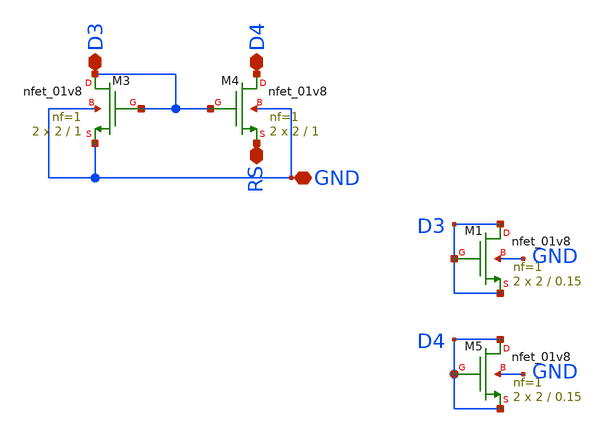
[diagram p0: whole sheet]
** sch_path: opamp/mag/nmoscs/nmoscs.sch
**.subckt nmoscs RS D3 D4 GND
*.iopin RS
*.iopin D3
*.iopin D4
*.iopin GND
XM3 D3 D3 GND GND sky130_fd_pr__nfet_01v8 L=1 W=2 nf=1 ad='int((nf+1)/2) * W/nf * 0.29' as='int((nf+2)/2) * W/nf * 0.29'
+ pd='2*int((nf+1)/2) * (W/nf + 0.29)' ps='2*int((nf+2)/2) * (W/nf + 0.29)' nrd='0.29 / W' nrs='0.29 / W'
+ sa=0 sb=0 sd=0 mult=2 m=2
XM4 D4 D3 RS GND sky130_fd_pr__nfet_01v8 L=1 W=2 nf=1 ad='int((nf+1)/2) * W/nf * 0.29' as='int((nf+2)/2) * W/nf * 0.29'
+ pd='2*int((nf+1)/2) * (W/nf + 0.29)' ps='2*int((nf+2)/2) * (W/nf + 0.29)' nrd='0.29 / W' nrs='0.29 / W'
+ sa=0 sb=0 sd=0 mult=2 m=2
XM1 D3 D3 D3 GND sky130_fd_pr__nfet_01v8 L=0.15 W=2 nf=1 ad='int((nf+1)/2) * W/nf * 0.29' as='int((nf+2)/2) * W/nf * 0.29'
+ pd='2*int((nf+1)/2) * (W/nf + 0.29)' ps='2*int((nf+2)/2) * (W/nf + 0.29)' nrd='0.29 / W' nrs='0.29 / W'
+ sa=0 sb=0 sd=0 mult=2 m=2
XM5 D4 D4 D4 GND sky130_fd_pr__nfet_01v8 L=0.15 W=2 nf=1 ad='int((nf+1)/2) * W/nf * 0.29' as='int((nf+2)/2) * W/nf * 0.29'
+ pd='2*int((nf+1)/2) * (W/nf + 0.29)' ps='2*int((nf+2)/2) * (W/nf + 0.29)' nrd='0.29 / W' nrs='0.29 / W'
+ sa=0 sb=0 sd=0 mult=2 m=2
**.ends
.end
